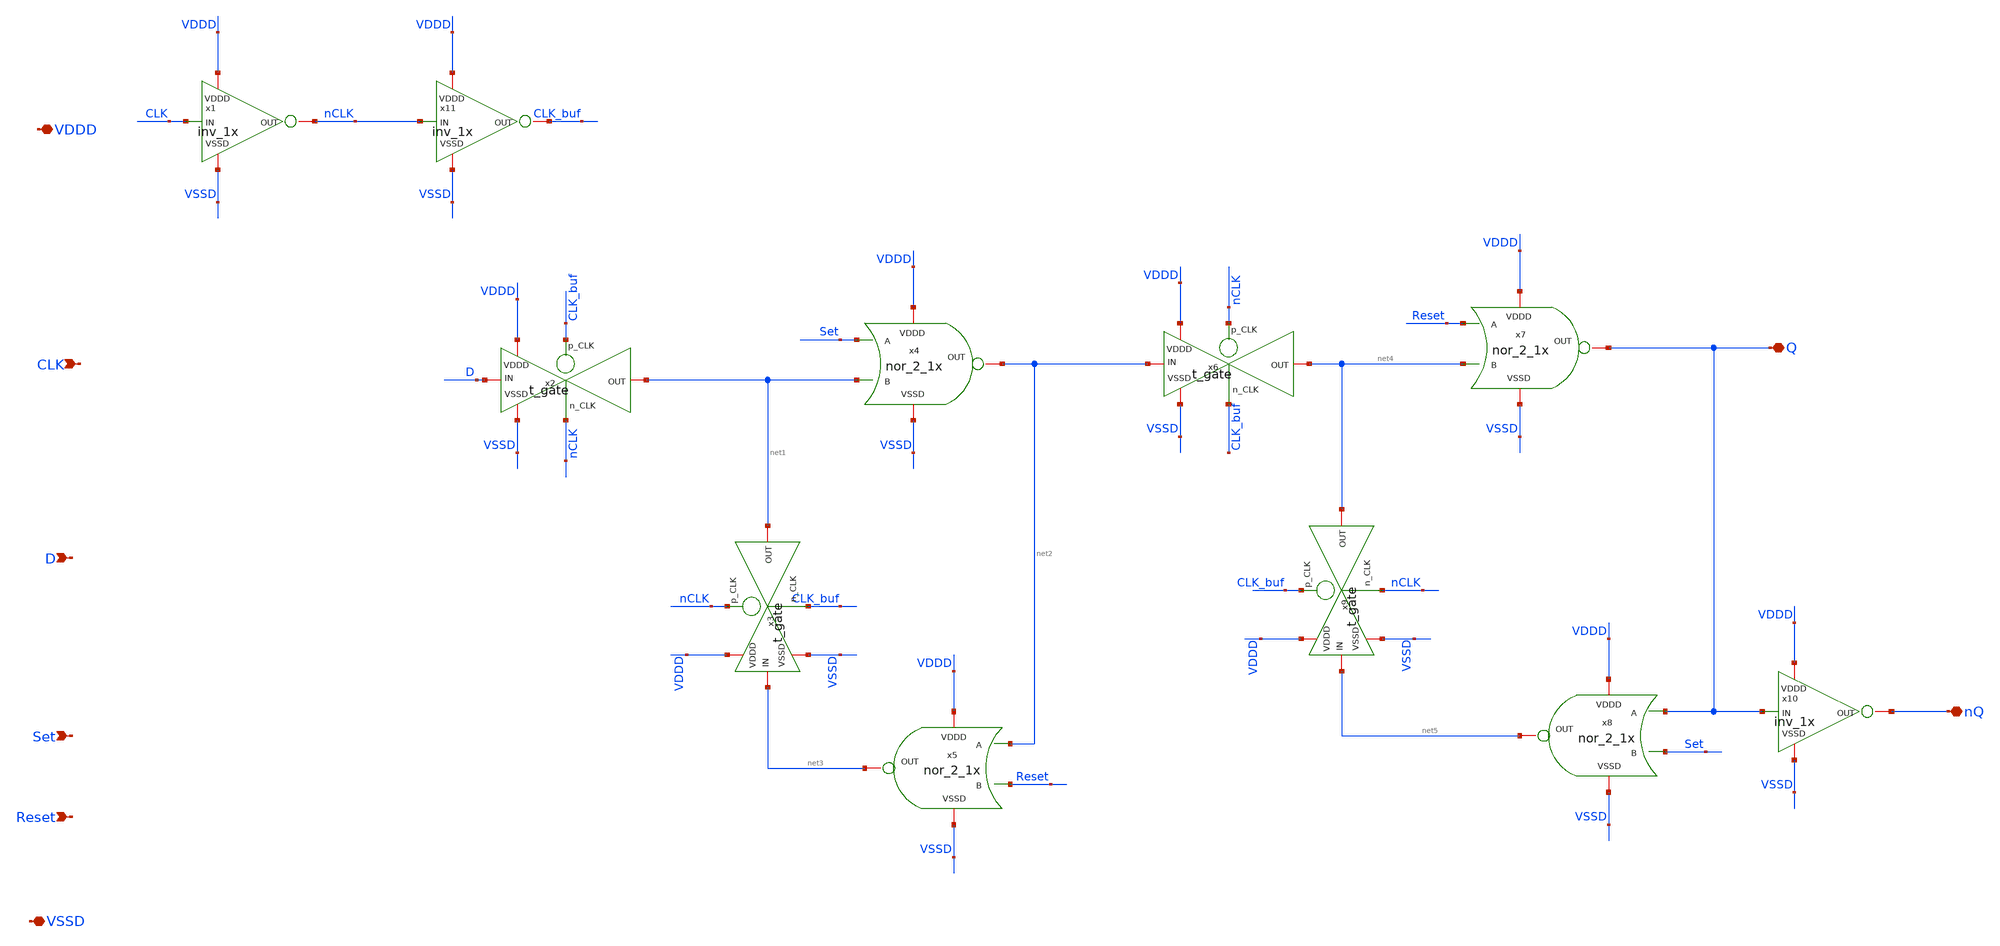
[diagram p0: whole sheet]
** sch_path: SAR_ADC/SAR_Asynchronous_Logic/xschem/SAR_Asynchronous_Logic_D_reset_FF.sch
**.subckt SAR_Asynchronous_Logic_D_reset_FF VDDD VSSD Q nQ CLK D Reset Set
*.iopin VDDD
*.iopin VSSD
*.iopin Q
*.iopin nQ
*.ipin CLK
*.ipin D
*.ipin Reset
*.ipin Set
x1 VDDD CLK nCLK VSSD inv_1x
x11 VDDD nCLK CLK_buf VSSD inv_1x
x2 CLK_buf VDDD D net1 VSSD nCLK t_gate
x4 VDDD Set net2 net1 VSSD nor_2_1x
x6 nCLK VDDD net2 net4 VSSD CLK_buf t_gate
x7 VDDD Reset Q net4 VSSD nor_2_1x
x3 nCLK VDDD net3 net1 VSSD CLK_buf t_gate
x9 CLK_buf VDDD net5 net4 VSSD nCLK t_gate
x5 VDDD net2 net3 Reset VSSD nor_2_1x
x8 VDDD Q net5 Set VSSD nor_2_1x
x10 VDDD Q nQ VSSD inv_1x
**.ends
.end
